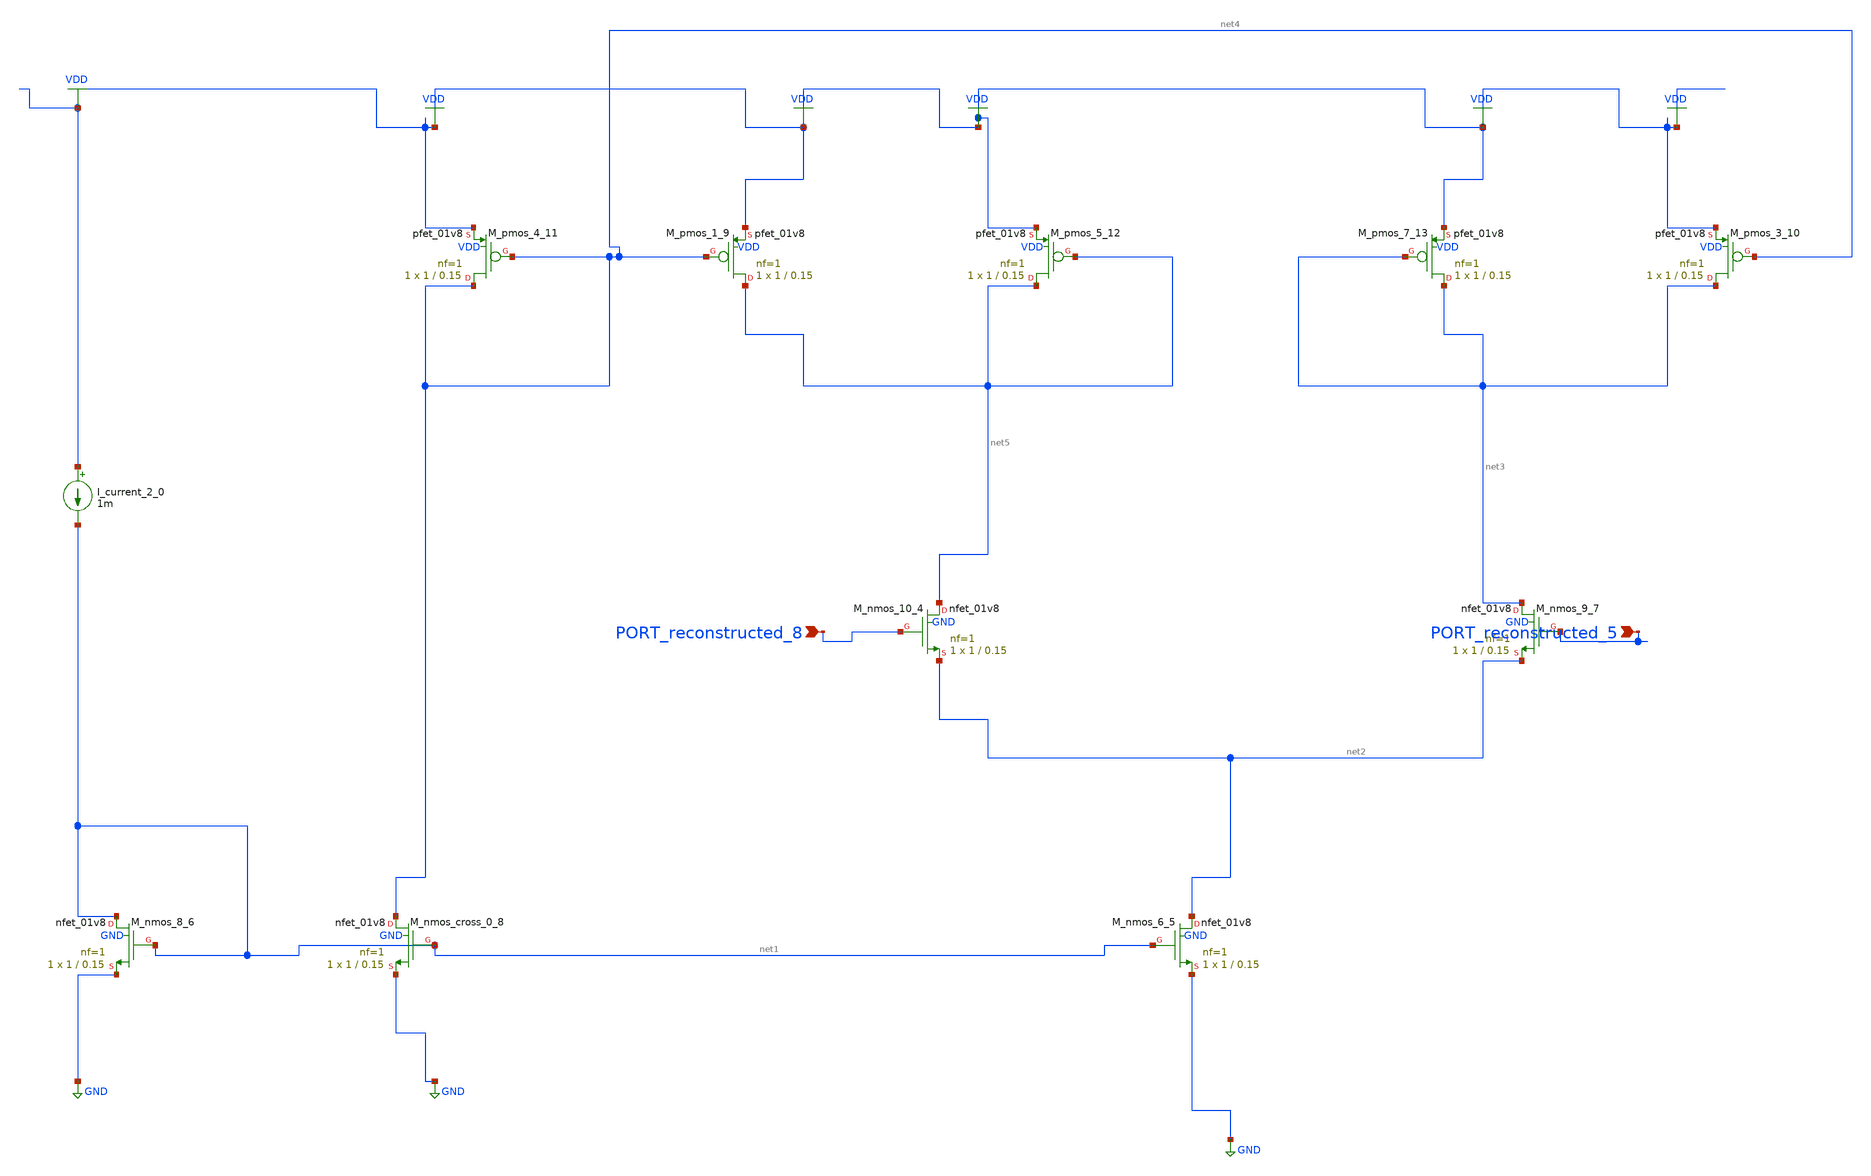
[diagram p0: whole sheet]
** sch_path: schematics/AMSNet/255.sch
**.subckt 255 PORT_reconstructed_5 PORT_reconstructed_8
*.ipin PORT_reconstructed_5
*.ipin PORT_reconstructed_8
I_current_2_0 VDD net1 1m
XM_nmos_10_4 net5 PORT_reconstructed_8 net2 GND sky130_fd_pr__nfet_01v8 L=0.15 W=1 nf=1 ad='int((1 + 1)/2) * 1 / 1 * 0.29'
+ as='int((1 + 2)/2) * 1 / 1 * 0.29' pd='2*int((1 + 1)/2) * (1 / 1 + 0.29)' ps='2*int((1 + 2)/2) * (1 / 1 + 0.29)'
+ nrd='0.29 / 1 ' nrs='0.29 / 1 ' sa=0 sb=0 sd=0 mult=1 m=1
XM_nmos_6_5 net2 net1 GND GND sky130_fd_pr__nfet_01v8 L=0.15 W=1 nf=1 ad='int((1 + 1)/2) * 1 / 1 * 0.29'
+ as='int((1 + 2)/2) * 1 / 1 * 0.29' pd='2*int((1 + 1)/2) * (1 / 1 + 0.29)' ps='2*int((1 + 2)/2) * (1 / 1 + 0.29)'
+ nrd='0.29 / 1 ' nrs='0.29 / 1 ' sa=0 sb=0 sd=0 mult=1 m=1
XM_nmos_8_6 net1 net1 GND GND sky130_fd_pr__nfet_01v8 L=0.15 W=1 nf=1 ad='int((1 + 1)/2) * 1 / 1 * 0.29'
+ as='int((1 + 2)/2) * 1 / 1 * 0.29' pd='2*int((1 + 1)/2) * (1 / 1 + 0.29)' ps='2*int((1 + 2)/2) * (1 / 1 + 0.29)'
+ nrd='0.29 / 1 ' nrs='0.29 / 1 ' sa=0 sb=0 sd=0 mult=1 m=1
XM_nmos_9_7 net3 PORT_reconstructed_5 net2 GND sky130_fd_pr__nfet_01v8 L=0.15 W=1 nf=1 ad='int((1 + 1)/2) * 1 / 1 * 0.29'
+ as='int((1 + 2)/2) * 1 / 1 * 0.29' pd='2*int((1 + 1)/2) * (1 / 1 + 0.29)' ps='2*int((1 + 2)/2) * (1 / 1 + 0.29)'
+ nrd='0.29 / 1 ' nrs='0.29 / 1 ' sa=0 sb=0 sd=0 mult=1 m=1
XM_nmos_cross_0_8 net4 net1 GND GND sky130_fd_pr__nfet_01v8 L=0.15 W=1 nf=1 ad='int((1 + 1)/2) * 1 / 1 * 0.29'
+ as='int((1 + 2)/2) * 1 / 1 * 0.29' pd='2*int((1 + 1)/2) * (1 / 1 + 0.29)' ps='2*int((1 + 2)/2) * (1 / 1 + 0.29)'
+ nrd='0.29 / 1 ' nrs='0.29 / 1 ' sa=0 sb=0 sd=0 mult=1 m=1
XM_pmos_1_9 net5 net4 VDD VDD sky130_fd_pr__pfet_01v8 L=0.15 W=1 nf=1 ad='int((1 + 1)/2) * 1 / 1 * 0.29'
+ as='int((1 + 2)/2) * 1 / 1 * 0.29' pd='2*int((1 + 1)/2) * (1 / 1 + 0.29)' ps='2*int((1 + 2)/2) * (1 / 1 + 0.29)'
+ nrd='0.29 / 1 ' nrs='0.29 / 1 ' sa=0 sb=0 sd=0 mult=1 m=1
XM_pmos_3_10 net3 net4 VDD VDD sky130_fd_pr__pfet_01v8 L=0.15 W=1 nf=1 ad='int((1 + 1)/2) * 1 / 1 * 0.29'
+ as='int((1 + 2)/2) * 1 / 1 * 0.29' pd='2*int((1 + 1)/2) * (1 / 1 + 0.29)' ps='2*int((1 + 2)/2) * (1 / 1 + 0.29)'
+ nrd='0.29 / 1 ' nrs='0.29 / 1 ' sa=0 sb=0 sd=0 mult=1 m=1
XM_pmos_4_11 net4 net4 VDD VDD sky130_fd_pr__pfet_01v8 L=0.15 W=1 nf=1 ad='int((1 + 1)/2) * 1 / 1 * 0.29'
+ as='int((1 + 2)/2) * 1 / 1 * 0.29' pd='2*int((1 + 1)/2) * (1 / 1 + 0.29)' ps='2*int((1 + 2)/2) * (1 / 1 + 0.29)'
+ nrd='0.29 / 1 ' nrs='0.29 / 1 ' sa=0 sb=0 sd=0 mult=1 m=1
XM_pmos_5_12 net5 net5 VDD VDD sky130_fd_pr__pfet_01v8 L=0.15 W=1 nf=1 ad='int((1 + 1)/2) * 1 / 1 * 0.29'
+ as='int((1 + 2)/2) * 1 / 1 * 0.29' pd='2*int((1 + 1)/2) * (1 / 1 + 0.29)' ps='2*int((1 + 2)/2) * (1 / 1 + 0.29)'
+ nrd='0.29 / 1 ' nrs='0.29 / 1 ' sa=0 sb=0 sd=0 mult=1 m=1
XM_pmos_7_13 net3 net3 VDD VDD sky130_fd_pr__pfet_01v8 L=0.15 W=1 nf=1 ad='int((1 + 1)/2) * 1 / 1 * 0.29'
+ as='int((1 + 2)/2) * 1 / 1 * 0.29' pd='2*int((1 + 1)/2) * (1 / 1 + 0.29)' ps='2*int((1 + 2)/2) * (1 / 1 + 0.29)'
+ nrd='0.29 / 1 ' nrs='0.29 / 1 ' sa=0 sb=0 sd=0 mult=1 m=1
**.ends
.GLOBAL GND
.GLOBAL VDD
.end
